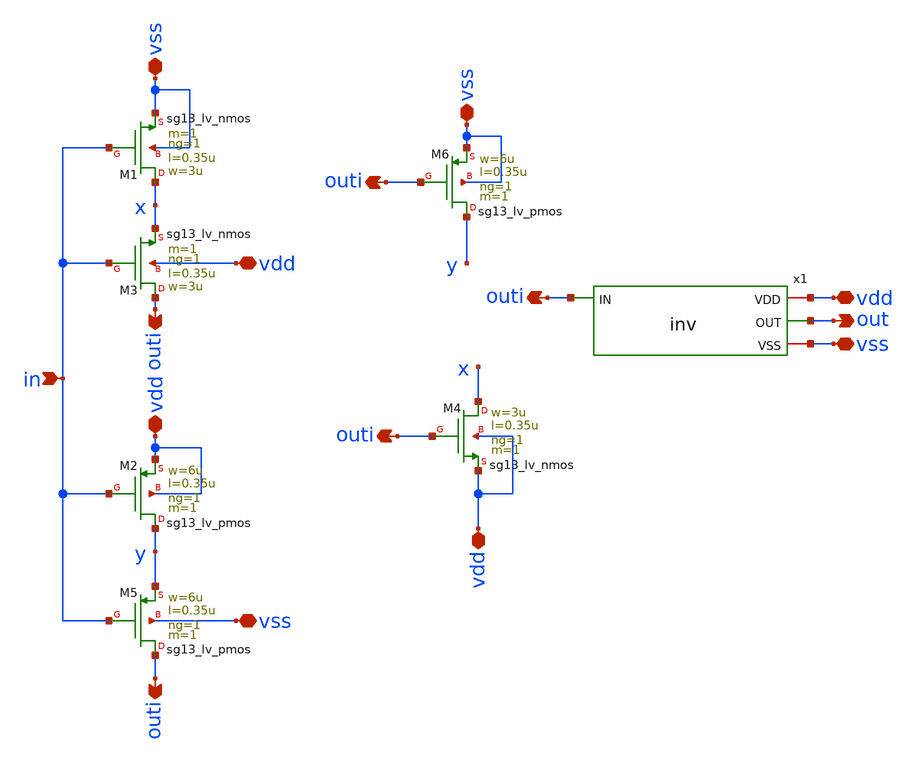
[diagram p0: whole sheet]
** sch_path: macros/heichips26_chronosense/schematic/xschem/schmitt.sch
* macros/heichips26_chronosense/schematic/xschem/inv.sch:
* Copyright 2023 IHP PDK Authors
* Licensed under the Apache License, Version 2.0 (the "License");
**.subckt schmitt vdd vdd vss in outi outi vss outi vdd outi outi vss vdd vss out
*.iopin vdd
*.iopin vdd
*.iopin vss
*.ipin in
*.opin outi
*.opin outi
*.iopin vss
*.opin outi
*.iopin vdd
*.opin outi
*.opin outi
*.iopin vss
*.iopin vdd
*.iopin vss
*.opin out
XM1 x in vss vss sg13_lv_nmos w=3u l=0.35u ng=1 m=1 mm_ok=1
XM2 y in vdd vdd sg13_lv_pmos w=6u l=0.35u ng=1 m=1 mm_ok=1
XM3 outi in x vdd sg13_lv_nmos w=3u l=0.35u ng=1 m=1 mm_ok=1
XM4 x outi vdd vdd sg13_lv_nmos w=3u l=0.35u ng=1 m=1 mm_ok=1
XM5 outi in y vss sg13_lv_pmos w=6u l=0.35u ng=1 m=1 mm_ok=1
XM6 y outi vss vss sg13_lv_pmos w=6u l=0.35u ng=1 m=1 mm_ok=1
x1 vdd outi out vss inv
**.ends

* expanding   symbol:  inv.sym # of pins=4
** sym_path: macros/heichips26_chronosense/schematic/xschem/inv.sym
** sch_path: macros/heichips26_chronosense/schematic/xschem/inv.sch
.subckt inv VDD IN OUT VSS
*.ipin IN
*.opin OUT
*.iopin VDD
*.iopin VSS
XM1 OUT IN VDD VDD sg13_lv_pmos w=2u l=0.35u ng=1 m=1 mm_ok=1
XM2 OUT IN VSS VSS sg13_lv_nmos w=1u l=0.35u ng=1 m=1 mm_ok=1
.ends

.end
